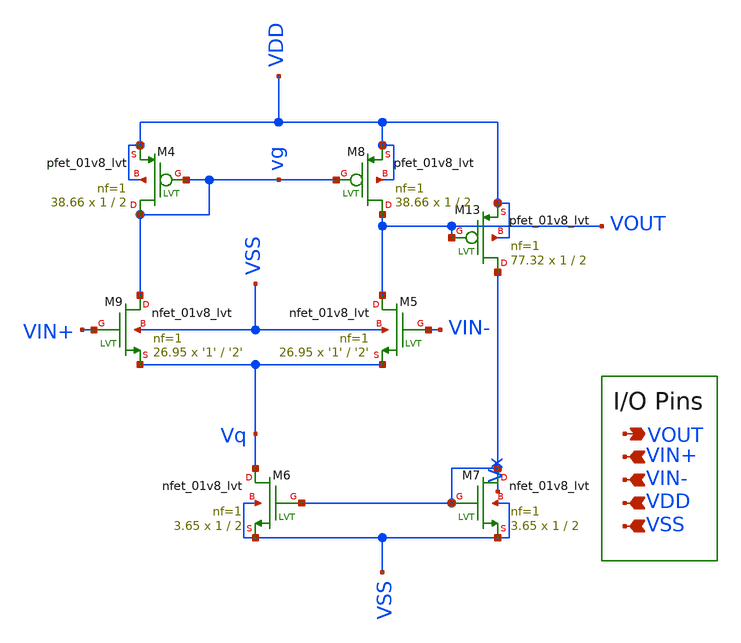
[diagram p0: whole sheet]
** sch_path: bandgap_sky130_v1/untitled-1.sch
**.subckt untitled-1 VOUT VIN+ VIN- VDD VSS
*.opin VOUT
*.ipin VIN+
*.ipin VIN-
*.ipin VDD
*.ipin VSS
XM5 VOUT VIN- Vq VSS sky130_fd_pr__nfet_01v8_lvt L='2' W='1' nf=1 ad='int((nf+1)/2) * W/nf * 0.29' as='int((nf+2)/2) * W/nf * 0.29'
+ pd='2*int((nf+1)/2) * (W/nf + 0.29)' ps='2*int((nf+2)/2) * (W/nf + 0.29)' nrd='0.29 / W' nrs='0.29 / W'
+ sa=0 sb=0 sd=0 mult=26.95 m=26.95
XM6 Vq Vx VSS VSS sky130_fd_pr__nfet_01v8_lvt L=2 W=1 nf=1 ad='int((nf+1)/2) * W/nf * 0.29' as='int((nf+2)/2) * W/nf * 0.29'
+ pd='2*int((nf+1)/2) * (W/nf + 0.29)' ps='2*int((nf+2)/2) * (W/nf + 0.29)' nrd='0.29 / W' nrs='0.29 / W'
+ sa=0 sb=0 sd=0 mult=3.65 m=3.65
XM9 vg VIN+ Vq VSS sky130_fd_pr__nfet_01v8_lvt L='2' W='1' nf=1 ad='int((nf+1)/2) * W/nf * 0.29' as='int((nf+2)/2) * W/nf * 0.29'
+ pd='2*int((nf+1)/2) * (W/nf + 0.29)' ps='2*int((nf+2)/2) * (W/nf + 0.29)' nrd='0.29 / W' nrs='0.29 / W'
+ sa=0 sb=0 sd=0 mult=26.95 m=26.95
XM7 Vx Vx VSS VSS sky130_fd_pr__nfet_01v8_lvt L=2 W=1 nf=1 ad='int((nf+1)/2) * W/nf * 0.29' as='int((nf+2)/2) * W/nf * 0.29'
+ pd='2*int((nf+1)/2) * (W/nf + 0.29)' ps='2*int((nf+2)/2) * (W/nf + 0.29)' nrd='0.29 / W' nrs='0.29 / W'
+ sa=0 sb=0 sd=0 mult=3.65 m=3.65
XM13 Vx VOUT VDD VDD sky130_fd_pr__pfet_01v8_lvt L=2 W=1 nf=1 ad='int((nf+1)/2) * W/nf * 0.29' as='int((nf+2)/2) * W/nf * 0.29'
+ pd='2*int((nf+1)/2) * (W/nf + 0.29)' ps='2*int((nf+2)/2) * (W/nf + 0.29)' nrd='0.29 / W' nrs='0.29 / W'
+ sa=0 sb=0 sd=0 mult=77.32 m=77.32
XM4 vg vg VDD VDD sky130_fd_pr__pfet_01v8_lvt L=2 W=1 nf=1 ad='int((nf+1)/2) * W/nf * 0.29' as='int((nf+2)/2) * W/nf * 0.29'
+ pd='2*int((nf+1)/2) * (W/nf + 0.29)' ps='2*int((nf+2)/2) * (W/nf + 0.29)' nrd='0.29 / W' nrs='0.29 / W'
+ sa=0 sb=0 sd=0 mult=38.66 m=38.66
XM8 VOUT vg VDD VDD sky130_fd_pr__pfet_01v8_lvt L=2 W=1 nf=1 ad='int((nf+1)/2) * W/nf * 0.29' as='int((nf+2)/2) * W/nf * 0.29'
+ pd='2*int((nf+1)/2) * (W/nf + 0.29)' ps='2*int((nf+2)/2) * (W/nf + 0.29)' nrd='0.29 / W' nrs='0.29 / W'
+ sa=0 sb=0 sd=0 mult=38.66 m=38.66
**.ends
.end
